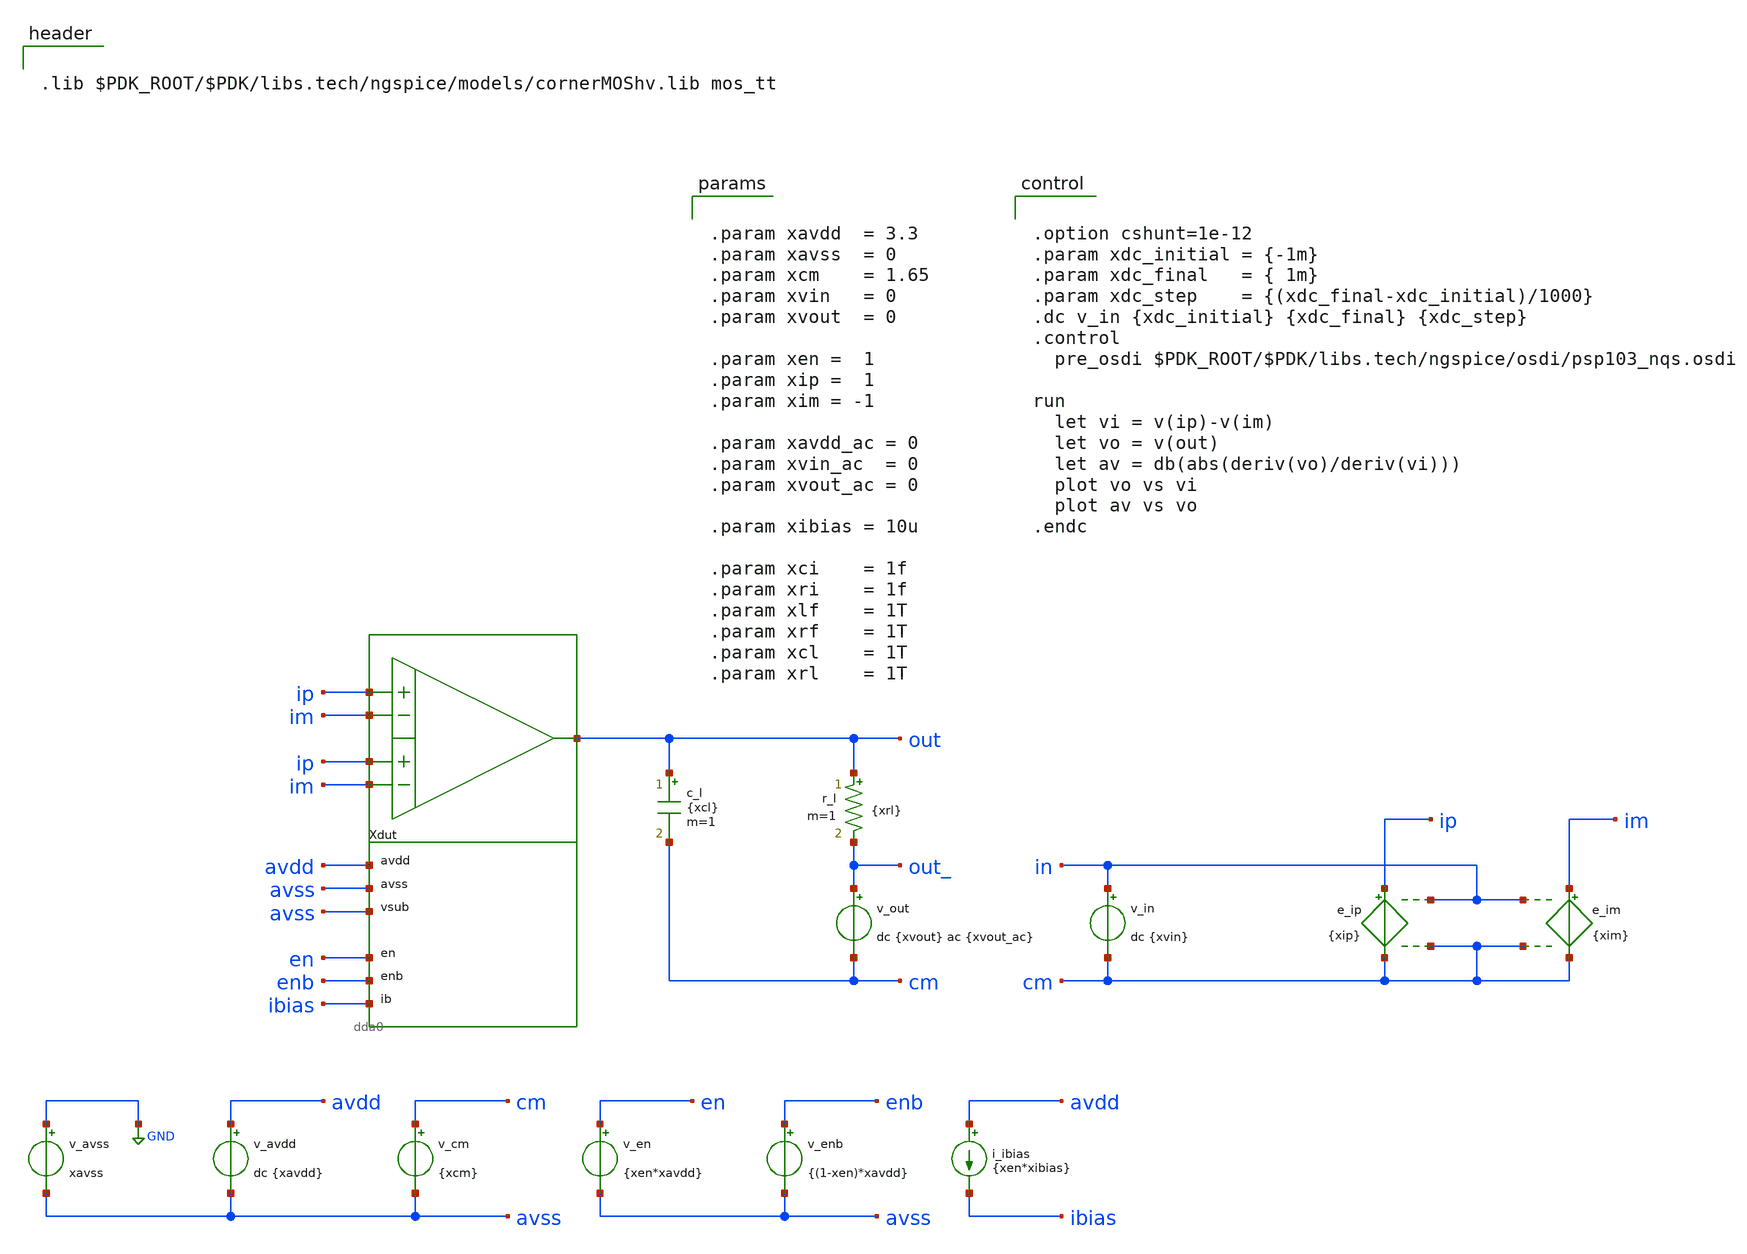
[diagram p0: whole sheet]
** sch_path: xschem/tb_dda0_open_dc.sch
**.subckt tb_dda0_open_dc
Xdut ip im ip im out avdd avss avss en enb ibias dda0
v_avss GND avss xavss
v_avdd avdd avss dc {xavdd}
v_in in cm dc {xvin}
v_en en avss {xen*xavdd}
v_enb enb avss {(1-xen)*xavdd}
i_ibias avdd ibias {xen*xibias}
c_l out cm {xcl} m=1
v_out out_ cm dc {xvout} ac {xvout_ac}
r_l out out_ {xrl} m=1
e_ip ip cm in cm {xip}
e_im im cm in cm {xim}
v_cm cm avss {xcm}
**** begin user architecture code


.lib $PDK_ROOT/$PDK/libs.tech/ngspice/models/cornerMOShv.lib mos_tt




.option cshunt=1e-12
.param xdc_initial = {-1m}
.param xdc_final   = { 1m}
.param xdc_step    = {(xdc_final-xdc_initial)/1000}
.dc v_in {xdc_initial} {xdc_final} {xdc_step}
.control
  pre_osdi $PDK_ROOT/$PDK/libs.tech/ngspice/osdi/psp103_nqs.osdi

run
  let vi = v(ip)-v(im)
  let vo = v(out)
  let av = db(abs(deriv(vo)/deriv(vi)))
  plot vo vs vi
  plot av vs vo
.endc




.param xavdd  = 3.3
.param xavss  = 0
.param xcm    = 1.65
.param xvin   = 0
.param xvout  = 0

.param xen =  1
.param xip =  1
.param xim = -1

.param xavdd_ac = 0
.param xvin_ac  = 0
.param xvout_ac = 0

.param xibias = 10u

.param xci    = 1f
.param xri    = 1f
.param xlf    = 1T
.param xrf    = 1T
.param xcl    = 1T
.param xrl    = 1T


**** end user architecture code
**.ends
.GLOBAL GND
.end
